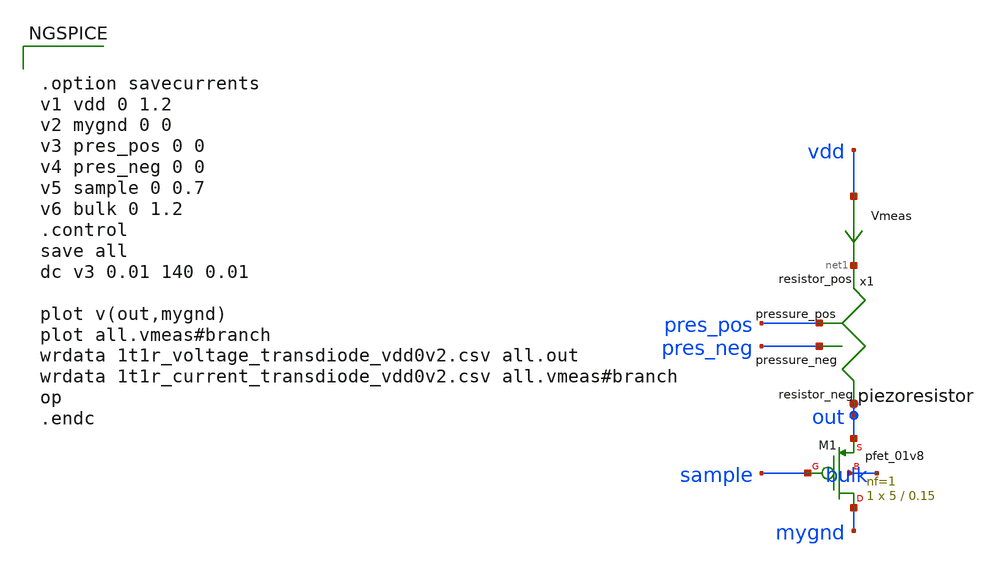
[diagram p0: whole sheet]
** sch_path: circuits/piezoresistive_synapse.sch
* Copyright 2020 Stefan Frederik Schippers
* Licensed under the Apache License, Version 2.0 (the "License");
* you may not use this file except in compliance with the License.
* You may obtain a copy of the License at
* https://www.apache.org/licenses/LICENSE-2.0
* Unless required by applicable law or agreed to in writing, software
* distributed under the License is distributed on an "AS IS" BASIS,
* WITHOUT WARRANTIES OR CONDITIONS OF ANY KIND, either express or implied.
* See the License for the specific language governing permissions and
* limitations under the License.
**.subckt piezoresistive_synapse
x1 pres_pos pres_neg net1 out piezoresistor
XM1 mygnd sample out bulk sky130_fd_pr__pfet_01v8 L=0.15 W=5 nf=1 ad='int((nf+1)/2) * W/nf * 0.29' as='int((nf+2)/2) * W/nf * 0.29'
+ pd='2*int((nf+1)/2) * (W/nf + 0.29)' ps='2*int((nf+2)/2) * (W/nf + 0.29)' nrd='0.29 / W' nrs='0.29 / W'
+ sa=0 sb=0 sd=0 mult=1 m=1
Vmeas vdd net1 0
.save i(vmeas)
**** begin user architecture code
 .lib $::SKYWATER_MODELS/models/sky130.lib.spice tt

.param mc_mm_switch=0
.param mc_pr_switch=1




.option savecurrents
v1 vdd 0 1.2
v2 mygnd 0 0
v3 pres_pos 0 0
v4 pres_neg 0 0
v5 sample 0 0.7
v6 bulk 0 1.2
.control
save all
dc v3 0.01 140 0.01

plot v(out,mygnd)
plot all.vmeas#branch
wrdata 1t1r_voltage_transdiode_vdd0v2.csv all.out
wrdata 1t1r_current_transdiode_vdd0v2.csv all.vmeas#branch
op
.endc


**** end user architecture code
**.ends

* expanding   symbol:  piezoresistor.sym # of pins=4
** sym_path: circuits/piezoresistor.sym
** sch_path: circuits/piezoresistor.sch
.subckt piezoresistor pressure_pos pressure_neg resistor_pos resistor_neg
*.ipin pressure_pos
*.ipin pressure_neg
*.iopin resistor_pos
*.iopin resistor_neg
Broot sqrtp 0 V = sqrt(v(pressure_pos,pressure_neg))
Bres res 0 V = 106*(50/v(sqrtp)-1)*exp(-0.328*v(sqrtp))+15
Brvar resistor_pos resistor_neg I = V(resistor_pos,resistor_neg)/V(res)
.ends

.end
